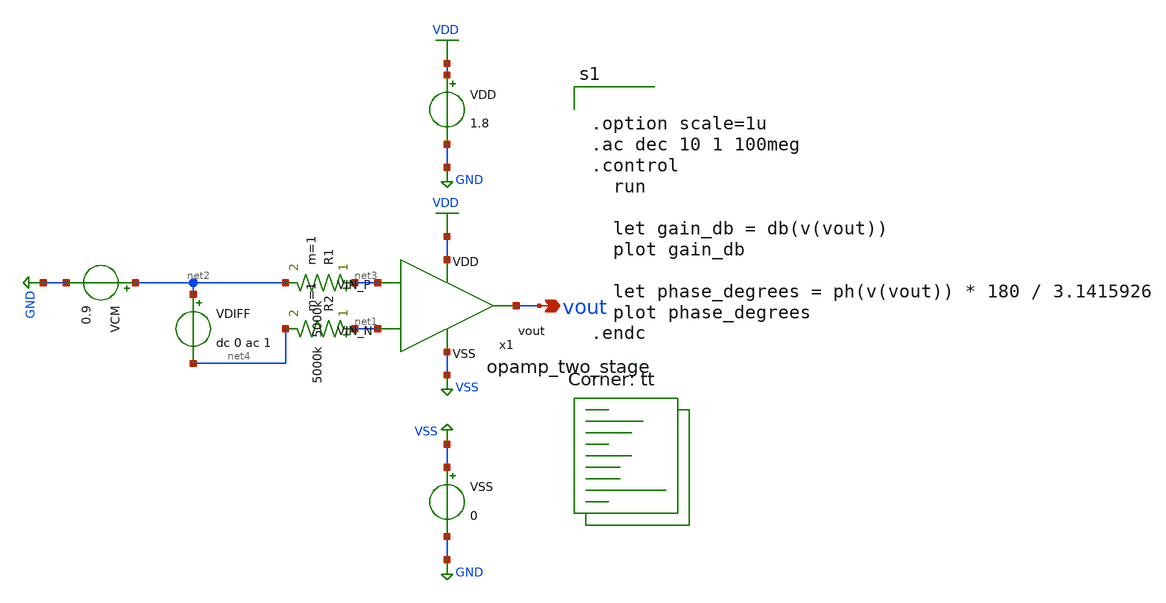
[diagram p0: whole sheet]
** sch_path: analog/schematics/tb_ac_analysis.sch
**.subckt tb_ac_analysis vout
*.opin vout
VDD VDD GND 1.8
VSS VSS GND 0
VCM net2 GND 0.9
VDIFF net2 net4 dc 0 ac 1
R1 net3 net2 5000k m=1
R2 net1 net4 5000k m=1
x1 VDD vout net3 net1 VSS opamp_two_stage
**** begin user architecture code


.option scale=1u
.ac dec 10 1 100meg
.control
  run

  let gain_db = db(v(vout))
  plot gain_db

  let phase_degrees = ph(v(vout)) * 180 / 3.1415926
  plot phase_degrees
.endc


.lib $::SKYWATER_MODELS/sky130.lib.spice tt
**** end user architecture code
**.ends

* expanding   symbol:  opamp_two_stage.sym # of pins=5
** sym_path: analog/schematics/opamp_two_stage.sym
** sch_path: analog/schematics/opamp_two_stage.sch
.subckt opamp_two_stage VDD vout VIN_P VIN_N VSS
*.ipin VIN_P
*.ipin VIN_N
*.opin vout
*.ipin VDD
*.ipin VSS
XM1 net3 VIN_N net4 VSS sky130_fd_pr__nfet_01v8 L=0.3 W=2 nf=1 ad='int((nf+1)/2) * W/nf * 0.29' as='int((nf+2)/2) * W/nf * 0.29'
+ pd='2*int((nf+1)/2) * (W/nf + 0.29)' ps='2*int((nf+2)/2) * (W/nf + 0.29)' nrd='0.29 / W' nrs='0.29 / W'
+ sa=0 sb=0 sd=0 mult=1 m=1
XM2 net5 VIN_P net4 VSS sky130_fd_pr__nfet_01v8 L=0.3 W=2 nf=1 ad='int((nf+1)/2) * W/nf * 0.29' as='int((nf+2)/2) * W/nf * 0.29'
+ pd='2*int((nf+1)/2) * (W/nf + 0.29)' ps='2*int((nf+2)/2) * (W/nf + 0.29)' nrd='0.29 / W' nrs='0.29 / W'
+ sa=0 sb=0 sd=0 mult=1 m=1
XM3 net3 net5 VDD VDD sky130_fd_pr__pfet_01v8 L=0.3 W=2 nf=1 ad='int((nf+1)/2) * W/nf * 0.29' as='int((nf+2)/2) * W/nf * 0.29'
+ pd='2*int((nf+1)/2) * (W/nf + 0.29)' ps='2*int((nf+2)/2) * (W/nf + 0.29)' nrd='0.29 / W' nrs='0.29 / W'
+ sa=0 sb=0 sd=0 mult=1 m=1
XM4 net5 net5 VDD VDD sky130_fd_pr__pfet_01v8 L=0.3 W=2 nf=1 ad='int((nf+1)/2) * W/nf * 0.29' as='int((nf+2)/2) * W/nf * 0.29'
+ pd='2*int((nf+1)/2) * (W/nf + 0.29)' ps='2*int((nf+2)/2) * (W/nf + 0.29)' nrd='0.29 / W' nrs='0.29 / W'
+ sa=0 sb=0 sd=0 mult=1 m=1
XM5 vout net3 VDD VDD sky130_fd_pr__pfet_01v8 L=0.3 W=2 nf=1 ad='int((nf+1)/2) * W/nf * 0.29' as='int((nf+2)/2) * W/nf * 0.29'
+ pd='2*int((nf+1)/2) * (W/nf + 0.29)' ps='2*int((nf+2)/2) * (W/nf + 0.29)' nrd='0.29 / W' nrs='0.29 / W'
+ sa=0 sb=0 sd=0 mult=2 m=2
XM6 vout net1 VSS VSS sky130_fd_pr__nfet_01v8 L=1 W=2 nf=1 ad='int((nf+1)/2) * W/nf * 0.29' as='int((nf+2)/2) * W/nf * 0.29'
+ pd='2*int((nf+1)/2) * (W/nf + 0.29)' ps='2*int((nf+2)/2) * (W/nf + 0.29)' nrd='0.29 / W' nrs='0.29 / W'
+ sa=0 sb=0 sd=0 mult=2 m=2
XM7 net4 net1 VSS VSS sky130_fd_pr__nfet_01v8 L=1 W=2 nf=1 ad='int((nf+1)/2) * W/nf * 0.29' as='int((nf+2)/2) * W/nf * 0.29'
+ pd='2*int((nf+1)/2) * (W/nf + 0.29)' ps='2*int((nf+2)/2) * (W/nf + 0.29)' nrd='0.29 / W' nrs='0.29 / W'
+ sa=0 sb=0 sd=0 mult=2 m=2
XR1 net3 net2 VSS sky130_fd_pr__res_high_po W=1 L=1 mult=1 m=1
XC1 vout net2 sky130_fd_pr__cap_mim_m3_1 W=1 L=1 MF=1 m=1
XR2 net1 VDD VSS sky130_fd_pr__res_high_po W=1 L=1 mult=1 m=1
XR3 VSS net1 VSS sky130_fd_pr__res_high_po W=1 L=1 mult=1 m=1
.ends

.GLOBAL VDD
.GLOBAL GND
.GLOBAL VSS
.end
